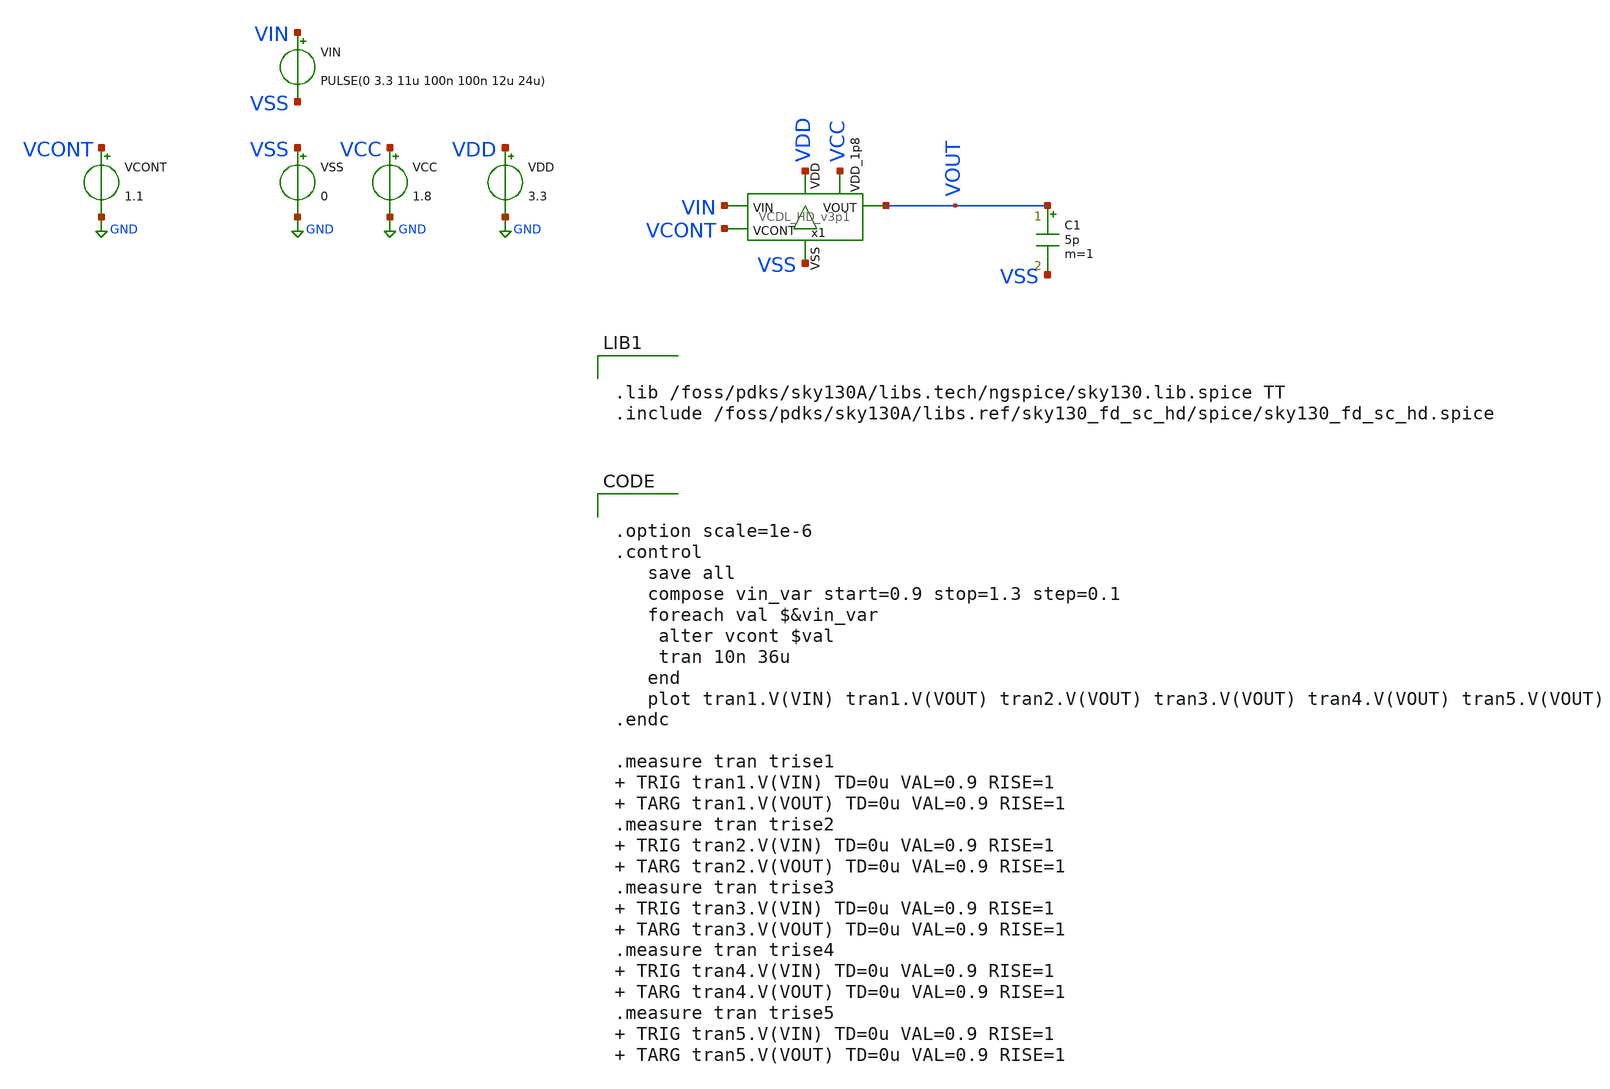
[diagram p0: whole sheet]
** sch_path: xschem/tb_VCDL_HD_v3p1.sch
**.subckt tb_VCDL_HD_v3p1
VCC VCC GND 1.8
VSS VSS GND 0
VIN VIN VSS PULSE(0 3.3 11u 100n 100n 12u 24u)
VCONT VCONT GND 1.1
C1 VOUT VSS 5p m=1
x1 VDD VCONT VOUT VIN VSS VCC VCDL_HD_v3p1
VDD VDD GND 3.3
**** begin user architecture code


.lib /foss/pdks/sky130A/libs.tech/ngspice/sky130.lib.spice TT
.include /foss/pdks/sky130A/libs.ref/sky130_fd_sc_hd/spice/sky130_fd_sc_hd.spice




.option scale=1e-6
.control
   save all
   compose vin_var start=0.9 stop=1.3 step=0.1
   foreach val $&vin_var
	alter vcont $val
	tran 10n 36u
   end
   plot tran1.V(VIN) tran1.V(VOUT) tran2.V(VOUT) tran3.V(VOUT) tran4.V(VOUT) tran5.V(VOUT)
.endc

.measure tran trise1   TRIG tran1.V(VIN) TD=0u VAL=0.9 RISE=1  TARG tran1.V(VOUT) TD=0u VAL=0.9
+ RISE=1
.measure tran trise2  TRIG tran2.V(VIN) TD=0u VAL=0.9 RISE=1  TARG tran2.V(VOUT) TD=0u VAL=0.9
+ RISE=1
.measure tran trise3  TRIG tran3.V(VIN) TD=0u VAL=0.9 RISE=1  TARG tran3.V(VOUT) TD=0u VAL=0.9
+ RISE=1
.measure tran trise4  TRIG tran4.V(VIN) TD=0u VAL=0.9 RISE=1  TARG tran4.V(VOUT) TD=0u VAL=0.9
+ RISE=1
.measure tran trise5  TRIG tran5.V(VIN) TD=0u VAL=0.9 RISE=1  TARG tran5.V(VOUT) TD=0u VAL=0.9
+ RISE=1


**** end user architecture code
**.ends
.GLOBAL GND
.end
